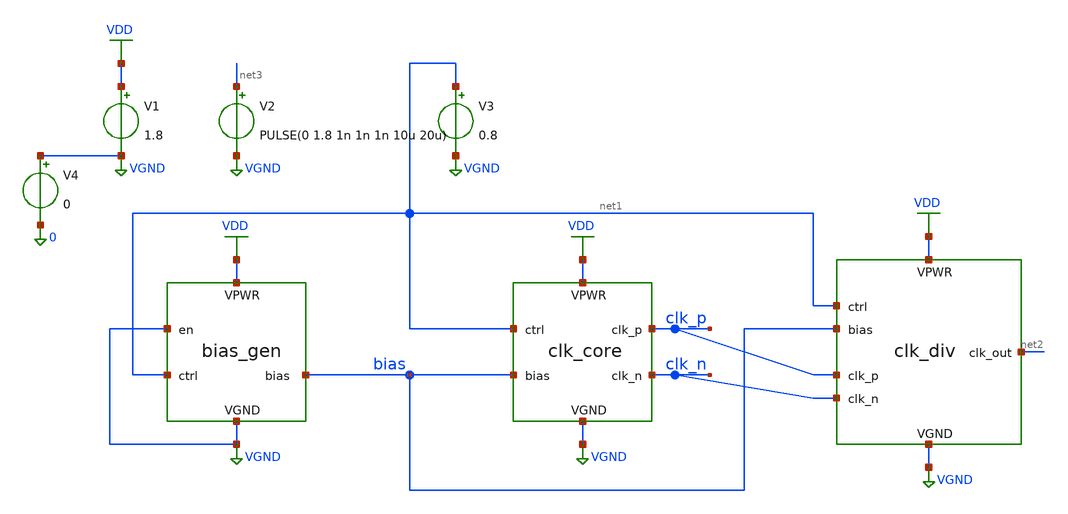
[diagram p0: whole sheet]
** sch_path: simple_vco/v1/tb_proto.sch
**.subckt tb_proto
x1 VDD VGND VGND net1 bias bias_gen
x2 VDD VGND net1 bias clk_p clk_n clk_core
x3 VDD VGND net1 bias clk_p clk_n net2 clk_div
V1 VDD VGND 1.8
V2 net3 VGND PULSE(0 1.8 1n 1n 1n 10u 20u)
V3 net1 VGND 0.8
V4 VGND 0 0
**** begin user architecture code


** opencircuitdesign pdks install

.lib $::SKYWATER_MODELS/sky130.lib.spice tt

.include $::SKYWATER_STDCELLS/sky130_fd_sc_hd.spice





.param mc_mm_switch=0

.control

save all

tran 5p 1u
*plot CLK_OUT CLK_P CLK_N
plot diff=par(clk_n - clk_p)
plot bias

*quit 0

.endc

.end



**** end user architecture code
**.ends

* expanding   symbol:  bias_gen.sym # of pins=5
** sym_path: simple_vco/v1/bias_gen.sym
** sch_path: simple_vco/v1/bias_gen.sch
.subckt bias_gen VPWR VGND en ctrl bias_out
*.iopin VPWR
*.iopin VGND
*.ipin en
*.ipin ctrl
*.opin bias_out
XM8 net5 net5 VPWR VPWR sky130_fd_pr__pfet_01v8 L=0.15 W=5 nf=1 ad='int((1 + 1)/2) * 5 / 1 * 0.29' as='int((1 + 2)/2) * 5 / 1 * 0.29'
+ pd='2*int((1 + 1)/2) * (5 / 1 + 0.29)' ps='2*int((1 + 2)/2) * (5 / 1 + 0.29)' nrd='0.29 / 5 ' nrs='0.29 / 5 '
+ sa=0 sb=0 sd=0 mult=1 m=1
XM7 bias_out ctrl net3 VPWR sky130_fd_pr__pfet_01v8 L=0.15 W=2 nf=1 ad='int((1 + 1)/2) * 2 / 1 * 0.29'
+ as='int((1 + 2)/2) * 2 / 1 * 0.29' pd='2*int((1 + 1)/2) * (2 / 1 + 0.29)' ps='2*int((1 + 2)/2) * (2 / 1 + 0.29)'
+ nrd='0.29 / 2 ' nrs='0.29 / 2 ' sa=0 sb=0 sd=0 mult=1 m=1
XM6 net4 net1 net3 VPWR sky130_fd_pr__pfet_01v8 L=0.15 W=2 nf=1 ad='int((1 + 1)/2) * 2 / 1 * 0.29' as='int((1 + 2)/2) * 2 / 1 * 0.29'
+ pd='2*int((1 + 1)/2) * (2 / 1 + 0.29)' ps='2*int((1 + 2)/2) * (2 / 1 + 0.29)' nrd='0.29 / 2 ' nrs='0.29 / 2 '
+ sa=0 sb=0 sd=0 mult=1 m=1
XM3 net1 ctrl VPWR VPWR sky130_fd_pr__pfet_01v8 L=0.15 W=5 nf=1 ad='int((1 + 1)/2) * 5 / 1 * 0.29' as='int((1 + 2)/2) * 5 / 1 * 0.29'
+ pd='2*int((1 + 1)/2) * (5 / 1 + 0.29)' ps='2*int((1 + 2)/2) * (5 / 1 + 0.29)' nrd='0.29 / 5 ' nrs='0.29 / 5 '
+ sa=0 sb=0 sd=0 mult=1 m=1
XM1 net1 net1 VPWR VPWR sky130_fd_pr__pfet_01v8 L=0.15 W=5 nf=1 ad='int((1 + 1)/2) * 5 / 1 * 0.29' as='int((1 + 2)/2) * 5 / 1 * 0.29'
+ pd='2*int((1 + 1)/2) * (5 / 1 + 0.29)' ps='2*int((1 + 2)/2) * (5 / 1 + 0.29)' nrd='0.29 / 5 ' nrs='0.29 / 5 '
+ sa=0 sb=0 sd=0 mult=1 m=1
XM5 net3 net5 VPWR VPWR sky130_fd_pr__pfet_01v8 L=0.15 W=5 nf=1 ad='int((1 + 1)/2) * 5 / 1 * 0.29' as='int((1 + 2)/2) * 5 / 1 * 0.29'
+ pd='2*int((1 + 1)/2) * (5 / 1 + 0.29)' ps='2*int((1 + 2)/2) * (5 / 1 + 0.29)' nrd='0.29 / 5 ' nrs='0.29 / 5 '
+ sa=0 sb=0 sd=0 mult=1 m=1
XM9 bias_out net4 VGND VGND sky130_fd_pr__nfet_01v8 L=0.15 W=5 nf=1 ad='int((1 + 1)/2) * 5 / 1 * 0.29'
+ as='int((1 + 2)/2) * 5 / 1 * 0.29' pd='2*int((1 + 1)/2) * (5 / 1 + 0.29)' ps='2*int((1 + 2)/2) * (5 / 1 + 0.29)'
+ nrd='0.29 / 5 ' nrs='0.29 / 5 ' sa=0 sb=0 sd=0 mult=1 m=1
XM10 net4 net4 VGND VGND sky130_fd_pr__nfet_01v8 L=0.15 W=5 nf=1 ad='int((1 + 1)/2) * 5 / 1 * 0.29' as='int((1 + 2)/2) * 5 / 1 * 0.29'
+ pd='2*int((1 + 1)/2) * (5 / 1 + 0.29)' ps='2*int((1 + 2)/2) * (5 / 1 + 0.29)' nrd='0.29 / 5 ' nrs='0.29 / 5 '
+ sa=0 sb=0 sd=0 mult=1 m=1
XM11 net5 VPWR net6 VGND sky130_fd_pr__nfet_01v8 L=0.15 W=2 nf=1 ad='int((1 + 1)/2) * 2 / 1 * 0.29' as='int((1 + 2)/2) * 2 / 1 * 0.29'
+ pd='2*int((1 + 1)/2) * (2 / 1 + 0.29)' ps='2*int((1 + 2)/2) * (2 / 1 + 0.29)' nrd='0.29 / 2 ' nrs='0.29 / 2 '
+ sa=0 sb=0 sd=0 mult=1 m=1
XM12 net6 bias_out VGND VGND sky130_fd_pr__nfet_01v8 L=0.15 W=5 nf=1 ad='int((1 + 1)/2) * 5 / 1 * 0.29'
+ as='int((1 + 2)/2) * 5 / 1 * 0.29' pd='2*int((1 + 1)/2) * (5 / 1 + 0.29)' ps='2*int((1 + 2)/2) * (5 / 1 + 0.29)'
+ nrd='0.29 / 5 ' nrs='0.29 / 5 ' sa=0 sb=0 sd=0 mult=1 m=1
XM13 net6 net7 VGND VGND sky130_fd_pr__nfet_01v8 L=0.15 W=5 nf=1 ad='int((1 + 1)/2) * 5 / 1 * 0.29' as='int((1 + 2)/2) * 5 / 1 * 0.29'
+ pd='2*int((1 + 1)/2) * (5 / 1 + 0.29)' ps='2*int((1 + 2)/2) * (5 / 1 + 0.29)' nrd='0.29 / 5 ' nrs='0.29 / 5 '
+ sa=0 sb=0 sd=0 mult=1 m=1
XM14 net7 net8 VPWR VPWR sky130_fd_pr__pfet_01v8 L=0.15 W=1 nf=1 ad='int((1 + 1)/2) * 1 / 1 * 0.29' as='int((1 + 2)/2) * 1 / 1 * 0.29'
+ pd='2*int((1 + 1)/2) * (1 / 1 + 0.29)' ps='2*int((1 + 2)/2) * (1 / 1 + 0.29)' nrd='0.29 / 1 ' nrs='0.29 / 1 '
+ sa=0 sb=0 sd=0 mult=1 m=1
XM15 net7 net8 VGND VGND sky130_fd_pr__nfet_01v8 L=0.15 W=1 nf=1 ad='int((1 + 1)/2) * 1 / 1 * 0.29' as='int((1 + 2)/2) * 1 / 1 * 0.29'
+ pd='2*int((1 + 1)/2) * (1 / 1 + 0.29)' ps='2*int((1 + 2)/2) * (1 / 1 + 0.29)' nrd='0.29 / 1 ' nrs='0.29 / 1 '
+ sa=0 sb=0 sd=0 mult=1 m=1
XM16 net8 net9 VPWR VPWR sky130_fd_pr__pfet_01v8 L=0.15 W=1 nf=1 ad='int((1 + 1)/2) * 1 / 1 * 0.29' as='int((1 + 2)/2) * 1 / 1 * 0.29'
+ pd='2*int((1 + 1)/2) * (1 / 1 + 0.29)' ps='2*int((1 + 2)/2) * (1 / 1 + 0.29)' nrd='0.29 / 1 ' nrs='0.29 / 1 '
+ sa=0 sb=0 sd=0 mult=1 m=1
XM17 net8 net9 VGND VGND sky130_fd_pr__nfet_01v8 L=0.15 W=1 nf=1 ad='int((1 + 1)/2) * 1 / 1 * 0.29' as='int((1 + 2)/2) * 1 / 1 * 0.29'
+ pd='2*int((1 + 1)/2) * (1 / 1 + 0.29)' ps='2*int((1 + 2)/2) * (1 / 1 + 0.29)' nrd='0.29 / 1 ' nrs='0.29 / 1 '
+ sa=0 sb=0 sd=0 mult=1 m=1
XM19 net9 bias_out VGND VGND sky130_fd_pr__nfet_01v8 L=0.15 W=1 nf=1 ad='int((1 + 1)/2) * 1 / 1 * 0.29'
+ as='int((1 + 2)/2) * 1 / 1 * 0.29' pd='2*int((1 + 1)/2) * (1 / 1 + 0.29)' ps='2*int((1 + 2)/2) * (1 / 1 + 0.29)'
+ nrd='0.29 / 1 ' nrs='0.29 / 1 ' sa=0 sb=0 sd=0 mult=1 m=1
XM18 net9 en VPWR VPWR sky130_fd_pr__pfet_01v8_hvt L=8 W=0.42 nf=1 ad='int((1 + 1)/2) * 0.42 / 1 * 0.29'
+ as='int((1 + 2)/2) * 0.42 / 1 * 0.29' pd='2*int((1 + 1)/2) * (0.42 / 1 + 0.29)' ps='2*int((1 + 2)/2) * (0.42 / 1 + 0.29)'
+ nrd='0.29 / 0.42 ' nrs='0.29 / 0.42 ' sa=0 sb=0 sd=0 mult=1 m=1
XM20 bias_out en VGND VGND sky130_fd_pr__nfet_01v8 L=0.15 W=0.42 nf=1 ad='int((1 + 1)/2) * 0.42 / 1 * 0.29'
+ as='int((1 + 2)/2) * 0.42 / 1 * 0.29' pd='2*int((1 + 1)/2) * (0.42 / 1 + 0.29)' ps='2*int((1 + 2)/2) * (0.42 / 1 + 0.29)'
+ nrd='0.29 / 0.42 ' nrs='0.29 / 0.42 ' sa=0 sb=0 sd=0 mult=1 m=1
XM21 net9 en VGND VGND sky130_fd_pr__nfet_01v8 L=0.15 W=0.42 nf=1 ad='int((1 + 1)/2) * 0.42 / 1 * 0.29'
+ as='int((1 + 2)/2) * 0.42 / 1 * 0.29' pd='2*int((1 + 1)/2) * (0.42 / 1 + 0.29)' ps='2*int((1 + 2)/2) * (0.42 / 1 + 0.29)'
+ nrd='0.29 / 0.42 ' nrs='0.29 / 0.42 ' sa=0 sb=0 sd=0 mult=1 m=1
XM4 net2 bias_out VGND VGND sky130_fd_pr__nfet_01v8 L=0.15 W=5 nf=1 ad='int((1 + 1)/2) * 5 / 1 * 0.29'
+ as='int((1 + 2)/2) * 5 / 1 * 0.29' pd='2*int((1 + 1)/2) * (5 / 1 + 0.29)' ps='2*int((1 + 2)/2) * (5 / 1 + 0.29)'
+ nrd='0.29 / 5 ' nrs='0.29 / 5 ' sa=0 sb=0 sd=0 mult=1 m=1
XM2 net1 VPWR net2 VGND sky130_fd_pr__nfet_01v8 L=0.15 W=2 nf=1 ad='int((1 + 1)/2) * 2 / 1 * 0.29' as='int((1 + 2)/2) * 2 / 1 * 0.29'
+ pd='2*int((1 + 1)/2) * (2 / 1 + 0.29)' ps='2*int((1 + 2)/2) * (2 / 1 + 0.29)' nrd='0.29 / 2 ' nrs='0.29 / 2 '
+ sa=0 sb=0 sd=0 mult=1 m=1
.ends


* expanding   symbol:  clk_core.sym # of pins=6
** sym_path: simple_vco/v1/clk_core.sym
** sch_path: simple_vco/v1/clk_core.sch
.subckt clk_core VPWR VGND ctrl bias_in clk_p clk_n
*.iopin VPWR
*.iopin VGND
*.ipin ctrl
*.ipin bias_in
*.opin clk_p
*.opin clk_n
**** begin user architecture code

.param WP=5 LP=0.15  WN_MAIN=2 LN_MAIN=0.15  WN_CC=0.42 LN_CC=0.15  WN_TAIL=5 LN_TAIL=0.15


**** end user architecture code
XM3 clk_p ctrl VPWR VPWR sky130_fd_pr__pfet_01v8 L=LP W=WP nf=1 ad='int((1 + 1)/2) * WP / 1 * 0.29' as='int((1 + 2)/2) * WP / 1 * 0.29'
+ pd='2*int((1 + 1)/2) * (WP / 1 + 0.29)' ps='2*int((1 + 2)/2) * (WP / 1 + 0.29)' nrd='0.29 / WP ' nrs='0.29 / WP '
+ sa=0 sb=0 sd=0 mult=1 m=1
XM1 clk_p clk_p VPWR VPWR sky130_fd_pr__pfet_01v8 L=LP W=WP nf=1 ad='int((1 + 1)/2) * WP / 1 * 0.29'
+ as='int((1 + 2)/2) * WP / 1 * 0.29' pd='2*int((1 + 1)/2) * (WP / 1 + 0.29)' ps='2*int((1 + 2)/2) * (WP / 1 + 0.29)'
+ nrd='0.29 / WP ' nrs='0.29 / WP ' sa=0 sb=0 sd=0 mult=1 m=1
XM4 net3 bias_in VGND VGND sky130_fd_pr__nfet_01v8 L=LN_TAIL W=WN_TAIL nf=1 ad='int((1 + 1)/2) * WN_TAIL / 1 * 0.29'
+ as='int((1 + 2)/2) * WN_TAIL / 1 * 0.29' pd='2*int((1 + 1)/2) * (WN_TAIL / 1 + 0.29)' ps='2*int((1 + 2)/2) * (WN_TAIL / 1 + 0.29)'
+ nrd='0.29 / WN_TAIL ' nrs='0.29 / WN_TAIL ' sa=0 sb=0 sd=0 mult=1 m=1
XM2 clk_p net1 net3 VGND sky130_fd_pr__nfet_01v8 L=LN_MAIN W=WN_MAIN nf=1 ad='int((1 + 1)/2) * WN_MAIN / 1 * 0.29'
+ as='int((1 + 2)/2) * WN_MAIN / 1 * 0.29' pd='2*int((1 + 1)/2) * (WN_MAIN / 1 + 0.29)' ps='2*int((1 + 2)/2) * (WN_MAIN / 1 + 0.29)'
+ nrd='0.29 / WN_MAIN ' nrs='0.29 / WN_MAIN ' sa=0 sb=0 sd=0 mult=1 m=1
XM5 clk_n ctrl VPWR VPWR sky130_fd_pr__pfet_01v8 L=LP W=WP nf=1 ad='int((1 + 1)/2) * WP / 1 * 0.29' as='int((1 + 2)/2) * WP / 1 * 0.29'
+ pd='2*int((1 + 1)/2) * (WP / 1 + 0.29)' ps='2*int((1 + 2)/2) * (WP / 1 + 0.29)' nrd='0.29 / WP ' nrs='0.29 / WP '
+ sa=0 sb=0 sd=0 mult=1 m=1
XM6 clk_n clk_n VPWR VPWR sky130_fd_pr__pfet_01v8 L=LP W=WP nf=1 ad='int((1 + 1)/2) * WP / 1 * 0.29'
+ as='int((1 + 2)/2) * WP / 1 * 0.29' pd='2*int((1 + 1)/2) * (WP / 1 + 0.29)' ps='2*int((1 + 2)/2) * (WP / 1 + 0.29)'
+ nrd='0.29 / WP ' nrs='0.29 / WP ' sa=0 sb=0 sd=0 mult=1 m=1
XM8 clk_n net2 net3 VGND sky130_fd_pr__nfet_01v8 L=LN_MAIN W=WN_MAIN nf=1 ad='int((1 + 1)/2) * WN_MAIN / 1 * 0.29'
+ as='int((1 + 2)/2) * WN_MAIN / 1 * 0.29' pd='2*int((1 + 1)/2) * (WN_MAIN / 1 + 0.29)' ps='2*int((1 + 2)/2) * (WN_MAIN / 1 + 0.29)'
+ nrd='0.29 / WN_MAIN ' nrs='0.29 / WN_MAIN ' sa=0 sb=0 sd=0 mult=1 m=1
XM7 clk_n clk_p net3 VGND sky130_fd_pr__nfet_01v8 L=LN_CC W=WN_CC nf=1 ad='int((1 + 1)/2) * WN_CC / 1 * 0.29'
+ as='int((1 + 2)/2) * WN_CC / 1 * 0.29' pd='2*int((1 + 1)/2) * (WN_CC / 1 + 0.29)' ps='2*int((1 + 2)/2) * (WN_CC / 1 + 0.29)'
+ nrd='0.29 / WN_CC ' nrs='0.29 / WN_CC ' sa=0 sb=0 sd=0 mult=1 m=1
XM9 clk_p clk_n net3 VGND sky130_fd_pr__nfet_01v8 L=LN_CC W=WN_CC nf=1 ad='int((1 + 1)/2) * WN_CC / 1 * 0.29'
+ as='int((1 + 2)/2) * WN_CC / 1 * 0.29' pd='2*int((1 + 1)/2) * (WN_CC / 1 + 0.29)' ps='2*int((1 + 2)/2) * (WN_CC / 1 + 0.29)'
+ nrd='0.29 / WN_CC ' nrs='0.29 / WN_CC ' sa=0 sb=0 sd=0 mult=1 m=1
XM10 net2 ctrl VPWR VPWR sky130_fd_pr__pfet_01v8 L=LP W=WP nf=1 ad='int((1 + 1)/2) * WP / 1 * 0.29' as='int((1 + 2)/2) * WP / 1 * 0.29'
+ pd='2*int((1 + 1)/2) * (WP / 1 + 0.29)' ps='2*int((1 + 2)/2) * (WP / 1 + 0.29)' nrd='0.29 / WP ' nrs='0.29 / WP '
+ sa=0 sb=0 sd=0 mult=1 m=1
XM11 net2 net2 VPWR VPWR sky130_fd_pr__pfet_01v8 L=LP W=WP nf=1 ad='int((1 + 1)/2) * WP / 1 * 0.29' as='int((1 + 2)/2) * WP / 1 * 0.29'
+ pd='2*int((1 + 1)/2) * (WP / 1 + 0.29)' ps='2*int((1 + 2)/2) * (WP / 1 + 0.29)' nrd='0.29 / WP ' nrs='0.29 / WP '
+ sa=0 sb=0 sd=0 mult=1 m=1
XM12 net4 bias_in VGND VGND sky130_fd_pr__nfet_01v8 L=LN_TAIL W=WN_TAIL nf=1 ad='int((1 + 1)/2) * WN_TAIL / 1 * 0.29'
+ as='int((1 + 2)/2) * WN_TAIL / 1 * 0.29' pd='2*int((1 + 1)/2) * (WN_TAIL / 1 + 0.29)' ps='2*int((1 + 2)/2) * (WN_TAIL / 1 + 0.29)'
+ nrd='0.29 / WN_TAIL ' nrs='0.29 / WN_TAIL ' sa=0 sb=0 sd=0 mult=1 m=1
XM13 net2 clk_p net4 VGND sky130_fd_pr__nfet_01v8 L=LN_MAIN W=WN_MAIN nf=1 ad='int((1 + 1)/2) * WN_MAIN / 1 * 0.29'
+ as='int((1 + 2)/2) * WN_MAIN / 1 * 0.29' pd='2*int((1 + 1)/2) * (WN_MAIN / 1 + 0.29)' ps='2*int((1 + 2)/2) * (WN_MAIN / 1 + 0.29)'
+ nrd='0.29 / WN_MAIN ' nrs='0.29 / WN_MAIN ' sa=0 sb=0 sd=0 mult=1 m=1
XM14 net1 ctrl VPWR VPWR sky130_fd_pr__pfet_01v8 L=LP W=WP nf=1 ad='int((1 + 1)/2) * WP / 1 * 0.29' as='int((1 + 2)/2) * WP / 1 * 0.29'
+ pd='2*int((1 + 1)/2) * (WP / 1 + 0.29)' ps='2*int((1 + 2)/2) * (WP / 1 + 0.29)' nrd='0.29 / WP ' nrs='0.29 / WP '
+ sa=0 sb=0 sd=0 mult=1 m=1
XM15 net1 net1 VPWR VPWR sky130_fd_pr__pfet_01v8 L=LP W=WP nf=1 ad='int((1 + 1)/2) * WP / 1 * 0.29' as='int((1 + 2)/2) * WP / 1 * 0.29'
+ pd='2*int((1 + 1)/2) * (WP / 1 + 0.29)' ps='2*int((1 + 2)/2) * (WP / 1 + 0.29)' nrd='0.29 / WP ' nrs='0.29 / WP '
+ sa=0 sb=0 sd=0 mult=1 m=1
XM16 net1 clk_n net4 VGND sky130_fd_pr__nfet_01v8 L=LN_MAIN W=WN_MAIN nf=1 ad='int((1 + 1)/2) * WN_MAIN / 1 * 0.29'
+ as='int((1 + 2)/2) * WN_MAIN / 1 * 0.29' pd='2*int((1 + 1)/2) * (WN_MAIN / 1 + 0.29)' ps='2*int((1 + 2)/2) * (WN_MAIN / 1 + 0.29)'
+ nrd='0.29 / WN_MAIN ' nrs='0.29 / WN_MAIN ' sa=0 sb=0 sd=0 mult=1 m=1
XM17 net1 net2 net4 VGND sky130_fd_pr__nfet_01v8 L=LN_CC W=WN_CC nf=1 ad='int((1 + 1)/2) * WN_CC / 1 * 0.29'
+ as='int((1 + 2)/2) * WN_CC / 1 * 0.29' pd='2*int((1 + 1)/2) * (WN_CC / 1 + 0.29)' ps='2*int((1 + 2)/2) * (WN_CC / 1 + 0.29)'
+ nrd='0.29 / WN_CC ' nrs='0.29 / WN_CC ' sa=0 sb=0 sd=0 mult=1 m=1
XM18 net2 net1 net4 VGND sky130_fd_pr__nfet_01v8 L=LN_CC W=WN_CC nf=1 ad='int((1 + 1)/2) * WN_CC / 1 * 0.29'
+ as='int((1 + 2)/2) * WN_CC / 1 * 0.29' pd='2*int((1 + 1)/2) * (WN_CC / 1 + 0.29)' ps='2*int((1 + 2)/2) * (WN_CC / 1 + 0.29)'
+ nrd='0.29 / WN_CC ' nrs='0.29 / WN_CC ' sa=0 sb=0 sd=0 mult=1 m=1
.ends


* expanding   symbol:  clk_div.sym # of pins=7
** sym_path: simple_vco/v1/clk_div.sym
** sch_path: simple_vco/v1/clk_div.sch
.subckt clk_div VPWR VGND ctrl bias_in clk_p clk_n clk_out
*.iopin VPWR
*.iopin VGND
*.ipin ctrl
*.ipin bias_in
*.ipin clk_p
*.ipin clk_n
*.opin clk_out
.ends

.GLOBAL VGND
.GLOBAL VDD
.end
